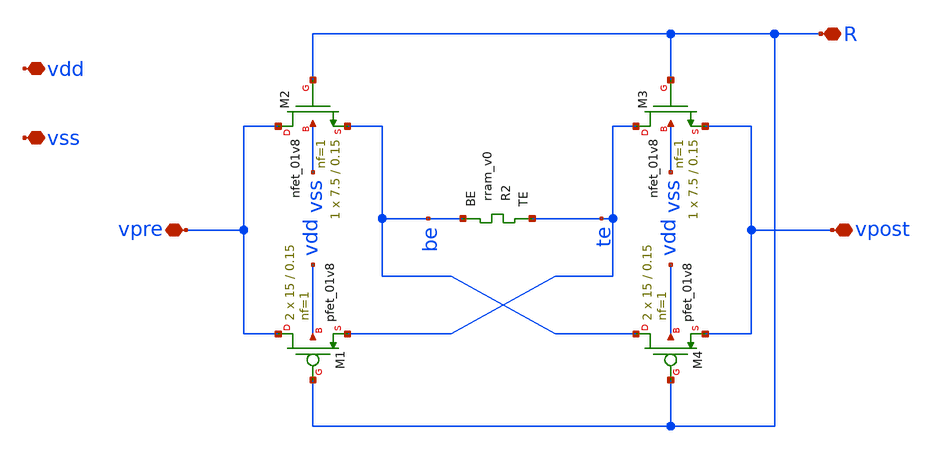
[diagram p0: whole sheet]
** sch_path: Synapse/rstdp.sch
**.subckt rstdp vdd vss R vpre vpost
*.iopin vdd
*.iopin vss
*.iopin R
*.iopin vpre
*.iopin vpost
XR2 te be rram_v0
XM2 vpre R be vss sky130_fd_pr__nfet_01v8 L=0.15 W=7.5 nf=1 ad='int((nf+1)/2) * W/nf * 0.29' as='int((nf+2)/2) * W/nf * 0.29'
+ pd='2*int((nf+1)/2) * (W/nf + 0.29)' ps='2*int((nf+2)/2) * (W/nf + 0.29)' nrd='0.29 / W' nrs='0.29 / W'
+ sa=0 sb=0 sd=0 mult=1 m=1
XM3 te R vpost vss sky130_fd_pr__nfet_01v8 L=0.15 W=7.5 nf=1 ad='int((nf+1)/2) * W/nf * 0.29' as='int((nf+2)/2) * W/nf * 0.29'
+ pd='2*int((nf+1)/2) * (W/nf + 0.29)' ps='2*int((nf+2)/2) * (W/nf + 0.29)' nrd='0.29 / W' nrs='0.29 / W'
+ sa=0 sb=0 sd=0 mult=1 m=1
XM1 vpre R te vdd sky130_fd_pr__pfet_01v8 L=0.15 W=15 nf=1 ad='int((nf+1)/2) * W/nf * 0.29' as='int((nf+2)/2) * W/nf * 0.29'
+ pd='2*int((nf+1)/2) * (W/nf + 0.29)' ps='2*int((nf+2)/2) * (W/nf + 0.29)' nrd='0.29 / W' nrs='0.29 / W'
+ sa=0 sb=0 sd=0 mult=2 m=2
XM4 be R vpost vdd sky130_fd_pr__pfet_01v8 L=0.15 W=15 nf=1 ad='int((nf+1)/2) * W/nf * 0.29' as='int((nf+2)/2) * W/nf * 0.29'
+ pd='2*int((nf+1)/2) * (W/nf + 0.29)' ps='2*int((nf+2)/2) * (W/nf + 0.29)' nrd='0.29 / W' nrs='0.29 / W'
+ sa=0 sb=0 sd=0 mult=2 m=2
**.ends
.end
